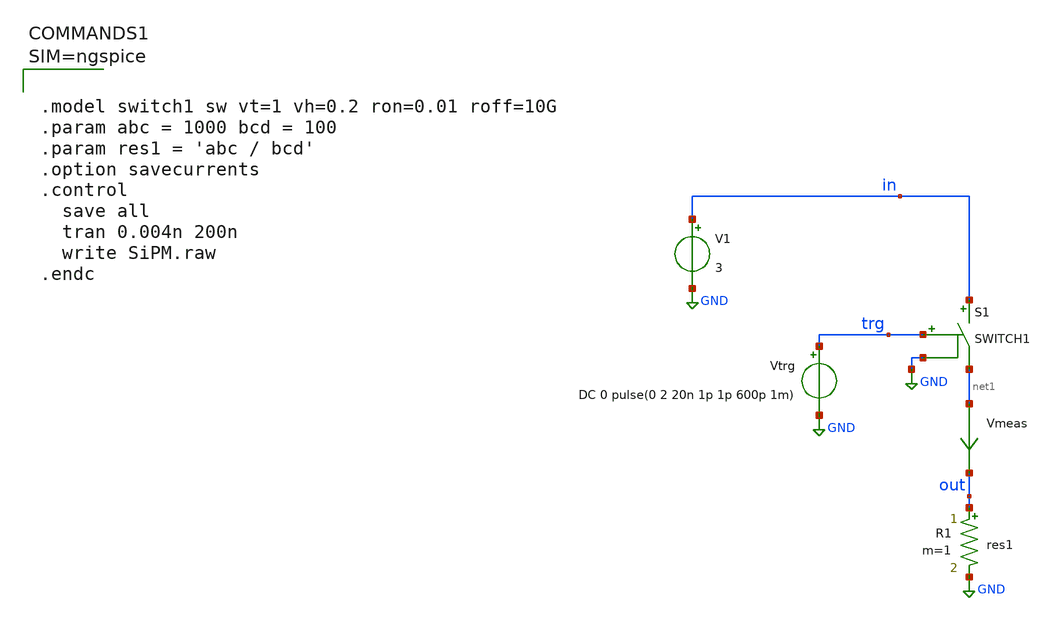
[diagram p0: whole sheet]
** sch_path: xschem/Test_SiPM.sch
**.subckt Test_SiPM
S1 in net1 trg GND SWITCH1
Vtrg trg GND DC 0 pulse(0 2 20n 1p 1p 600p 1m)
V1 in GND 3
Vmeas net1 out 0
.save i(vmeas)
R1 out GND res1 m=1
**** begin user architecture code



.model switch1 sw vt=1 vh=0.2 ron=0.01 roff=10G
.param abc = 1000 bcd = 100
.param res1 = 'abc / bcd'
.option savecurrents
.control
  save all
  tran 0.004n 200n
  write SiPM.raw
.endc



**** end user architecture code
**.ends
.GLOBAL GND
.end
